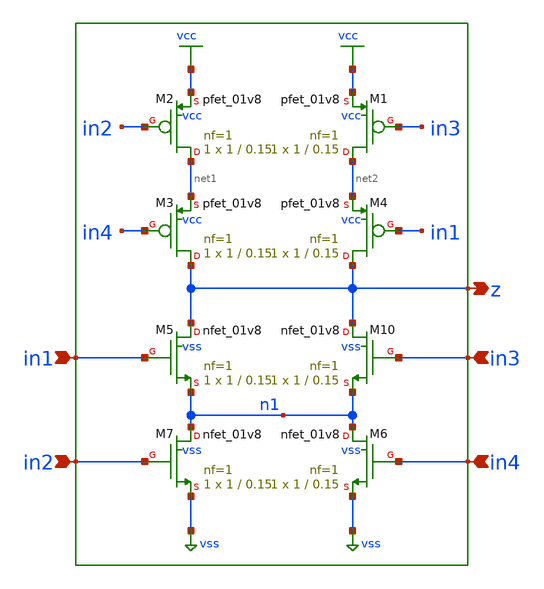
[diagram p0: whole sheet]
** sch_path: src/xe/test_cases/cplx.sch
**.subckt cplx in1 in2 in3 in4 z
*.ipin in1
*.ipin in2
*.ipin in3
*.ipin in4
*.opin z
XM2 net1 in2 vcc vcc sky130_fd_pr__pfet_01v8 L=0.15 W=1 nf=1 ad='int((nf+1)/2) * W/nf * 0.29' as='int((nf+2)/2) * W/nf * 0.29'
+ pd='2*int((nf+1)/2) * (W/nf + 0.29)' ps='2*int((nf+2)/2) * (W/nf + 0.29)' nrd='0.29 / W' nrs='0.29 / W'
+ sa=0 sb=0 sd=0 mult=1 m=1
XM10 z in3 n1 vss sky130_fd_pr__nfet_01v8 L=0.15 W=1 nf=1 ad='int((nf+1)/2) * W/nf * 0.29' as='int((nf+2)/2) * W/nf * 0.29'
+ pd='2*int((nf+1)/2) * (W/nf + 0.29)' ps='2*int((nf+2)/2) * (W/nf + 0.29)' nrd='0.29 / W' nrs='0.29 / W'
+ sa=0 sb=0 sd=0 mult=1 m=1
XM1 net2 in3 vcc vcc sky130_fd_pr__pfet_01v8 L=0.15 W=1 nf=1 ad='int((nf+1)/2) * W/nf * 0.29' as='int((nf+2)/2) * W/nf * 0.29'
+ pd='2*int((nf+1)/2) * (W/nf + 0.29)' ps='2*int((nf+2)/2) * (W/nf + 0.29)' nrd='0.29 / W' nrs='0.29 / W'
+ sa=0 sb=0 sd=0 mult=1 m=1
XM3 z in4 net1 vcc sky130_fd_pr__pfet_01v8 L=0.15 W=1 nf=1 ad='int((nf+1)/2) * W/nf * 0.29' as='int((nf+2)/2) * W/nf * 0.29'
+ pd='2*int((nf+1)/2) * (W/nf + 0.29)' ps='2*int((nf+2)/2) * (W/nf + 0.29)' nrd='0.29 / W' nrs='0.29 / W'
+ sa=0 sb=0 sd=0 mult=1 m=1
XM4 z in1 net2 vcc sky130_fd_pr__pfet_01v8 L=0.15 W=1 nf=1 ad='int((nf+1)/2) * W/nf * 0.29' as='int((nf+2)/2) * W/nf * 0.29'
+ pd='2*int((nf+1)/2) * (W/nf + 0.29)' ps='2*int((nf+2)/2) * (W/nf + 0.29)' nrd='0.29 / W' nrs='0.29 / W'
+ sa=0 sb=0 sd=0 mult=1 m=1
XM5 z in1 n1 vss sky130_fd_pr__nfet_01v8 L=0.15 W=1 nf=1 ad='int((nf+1)/2) * W/nf * 0.29' as='int((nf+2)/2) * W/nf * 0.29'
+ pd='2*int((nf+1)/2) * (W/nf + 0.29)' ps='2*int((nf+2)/2) * (W/nf + 0.29)' nrd='0.29 / W' nrs='0.29 / W'
+ sa=0 sb=0 sd=0 mult=1 m=1
XM6 n1 in4 vss vss sky130_fd_pr__nfet_01v8 L=0.15 W=1 nf=1 ad='int((nf+1)/2) * W/nf * 0.29' as='int((nf+2)/2) * W/nf * 0.29'
+ pd='2*int((nf+1)/2) * (W/nf + 0.29)' ps='2*int((nf+2)/2) * (W/nf + 0.29)' nrd='0.29 / W' nrs='0.29 / W'
+ sa=0 sb=0 sd=0 mult=1 m=1
XM7 n1 in2 vss vss sky130_fd_pr__nfet_01v8 L=0.15 W=1 nf=1 ad='int((nf+1)/2) * W/nf * 0.29' as='int((nf+2)/2) * W/nf * 0.29'
+ pd='2*int((nf+1)/2) * (W/nf + 0.29)' ps='2*int((nf+2)/2) * (W/nf + 0.29)' nrd='0.29 / W' nrs='0.29 / W'
+ sa=0 sb=0 sd=0 mult=1 m=1
**.ends
.GLOBAL vss
.GLOBAL vcc
.end
